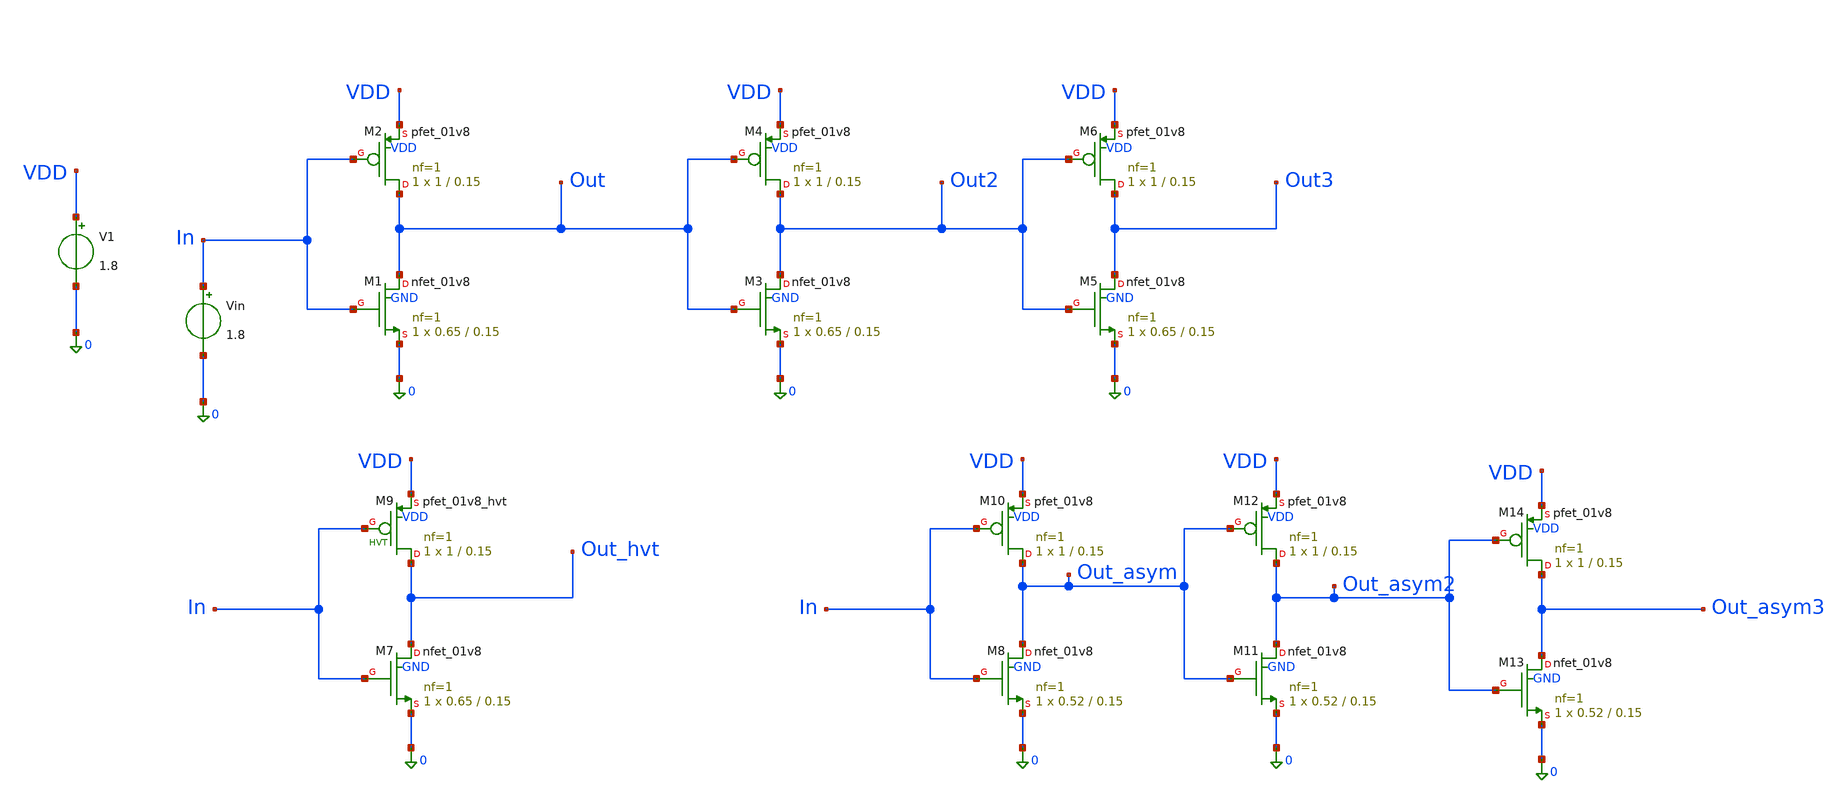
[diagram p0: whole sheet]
** sch_path: schem/inv_sizing.sch
**.subckt inv_sizing
XM1 Out In 0 GND sky130_fd_pr__nfet_01v8 L=0.15 W=0.65 nf=1 ad='int((1 + 1)/2) * 0.65 / 1 * 0.29' as='int((1 + 2)/2) * 0.65 / 1 * 0.29'
+ pd='2*int((1 + 1)/2) * (0.65 / 1 + 0.29)' ps='2*int((1 + 2)/2) * (0.65 / 1 + 0.29)' nrd='0.29 / 0.65 '
+ nrs='0.29 / 0.65 ' sa=0 sb=0 sd=0 mult=1 m=1
XM2 Out In VDD VDD sky130_fd_pr__pfet_01v8 L=0.15 W=1 nf=1 ad='int((1 + 1)/2) * 1 / 1 * 0.29' as='int((1 + 2)/2) * 1 / 1 * 0.29'
+ pd='2*int((1 + 1)/2) * (1 / 1 + 0.29)' ps='2*int((1 + 2)/2) * (1 / 1 + 0.29)' nrd='0.29 / 1 ' nrs='0.29 / 1 '
+ sa=0 sb=0 sd=0 mult=1 m=1
V1 VDD 0 1.8
Vin In 0 1.8
.save i(vin)
XM3 Out2 Out 0 GND sky130_fd_pr__nfet_01v8 L=0.15 W=0.65 nf=1 ad='int((1 + 1)/2) * 0.65 / 1 * 0.29' as='int((1 + 2)/2) * 0.65 / 1 * 0.29'
+ pd='2*int((1 + 1)/2) * (0.65 / 1 + 0.29)' ps='2*int((1 + 2)/2) * (0.65 / 1 + 0.29)' nrd='0.29 / 0.65 '
+ nrs='0.29 / 0.65 ' sa=0 sb=0 sd=0 mult=1 m=1
XM4 Out2 Out VDD VDD sky130_fd_pr__pfet_01v8 L=0.15 W=1 nf=1 ad='int((1 + 1)/2) * 1 / 1 * 0.29' as='int((1 + 2)/2) * 1 / 1 * 0.29'
+ pd='2*int((1 + 1)/2) * (1 / 1 + 0.29)' ps='2*int((1 + 2)/2) * (1 / 1 + 0.29)' nrd='0.29 / 1 ' nrs='0.29 / 1 '
+ sa=0 sb=0 sd=0 mult=1 m=1
XM5 Out3 Out2 0 GND sky130_fd_pr__nfet_01v8 L=0.15 W=0.65 nf=1 ad='int((1 + 1)/2) * 0.65 / 1 * 0.29'
+ as='int((1 + 2)/2) * 0.65 / 1 * 0.29' pd='2*int((1 + 1)/2) * (0.65 / 1 + 0.29)' ps='2*int((1 + 2)/2) * (0.65 / 1 + 0.29)'
+ nrd='0.29 / 0.65 ' nrs='0.29 / 0.65 ' sa=0 sb=0 sd=0 mult=1 m=1
XM6 Out3 Out2 VDD VDD sky130_fd_pr__pfet_01v8 L=0.15 W=1 nf=1 ad='int((1 + 1)/2) * 1 / 1 * 0.29' as='int((1 + 2)/2) * 1 / 1 * 0.29'
+ pd='2*int((1 + 1)/2) * (1 / 1 + 0.29)' ps='2*int((1 + 2)/2) * (1 / 1 + 0.29)' nrd='0.29 / 1 ' nrs='0.29 / 1 '
+ sa=0 sb=0 sd=0 mult=1 m=1
XM7 Out_hvt In 0 GND sky130_fd_pr__nfet_01v8 L=0.15 W=0.65 nf=1 ad='int((1 + 1)/2) * 0.65 / 1 * 0.29'
+ as='int((1 + 2)/2) * 0.65 / 1 * 0.29' pd='2*int((1 + 1)/2) * (0.65 / 1 + 0.29)' ps='2*int((1 + 2)/2) * (0.65 / 1 + 0.29)'
+ nrd='0.29 / 0.65 ' nrs='0.29 / 0.65 ' sa=0 sb=0 sd=0 mult=1 m=1
XM9 Out_hvt In VDD VDD sky130_fd_pr__pfet_01v8_hvt L=0.15 W=1 nf=1 ad='int((1 + 1)/2) * 1 / 1 * 0.29'
+ as='int((1 + 2)/2) * 1 / 1 * 0.29' pd='2*int((1 + 1)/2) * (1 / 1 + 0.29)' ps='2*int((1 + 2)/2) * (1 / 1 + 0.29)'
+ nrd='0.29 / 1 ' nrs='0.29 / 1 ' sa=0 sb=0 sd=0 mult=1 m=1
XM8 Out_asym In 0 GND sky130_fd_pr__nfet_01v8 L=0.15 W=0.52 nf=1 ad='int((1 + 1)/2) * 0.52 / 1 * 0.29'
+ as='int((1 + 2)/2) * 0.52 / 1 * 0.29' pd='2*int((1 + 1)/2) * (0.52 / 1 + 0.29)' ps='2*int((1 + 2)/2) * (0.52 / 1 + 0.29)'
+ nrd='0.29 / 0.52 ' nrs='0.29 / 0.52 ' sa=0 sb=0 sd=0 mult=1 m=1
XM10 Out_asym In VDD VDD sky130_fd_pr__pfet_01v8 L=0.15 W=1 nf=1 ad='int((1 + 1)/2) * 1 / 1 * 0.29' as='int((1 + 2)/2) * 1 / 1 * 0.29'
+ pd='2*int((1 + 1)/2) * (1 / 1 + 0.29)' ps='2*int((1 + 2)/2) * (1 / 1 + 0.29)' nrd='0.29 / 1 ' nrs='0.29 / 1 '
+ sa=0 sb=0 sd=0 mult=1 m=1
XM11 Out_asym2 Out_asym 0 GND sky130_fd_pr__nfet_01v8 L=0.15 W=0.52 nf=1 ad='int((1 + 1)/2) * 0.52 / 1 * 0.29'
+ as='int((1 + 2)/2) * 0.52 / 1 * 0.29' pd='2*int((1 + 1)/2) * (0.52 / 1 + 0.29)' ps='2*int((1 + 2)/2) * (0.52 / 1 + 0.29)'
+ nrd='0.29 / 0.52 ' nrs='0.29 / 0.52 ' sa=0 sb=0 sd=0 mult=1 m=1
XM12 Out_asym2 Out_asym VDD VDD sky130_fd_pr__pfet_01v8 L=0.15 W=1 nf=1 ad='int((1 + 1)/2) * 1 / 1 * 0.29'
+ as='int((1 + 2)/2) * 1 / 1 * 0.29' pd='2*int((1 + 1)/2) * (1 / 1 + 0.29)' ps='2*int((1 + 2)/2) * (1 / 1 + 0.29)'
+ nrd='0.29 / 1 ' nrs='0.29 / 1 ' sa=0 sb=0 sd=0 mult=1 m=1
XM13 Out_asym3 Out_asym2 0 GND sky130_fd_pr__nfet_01v8 L=0.15 W=0.52 nf=1 ad='int((1 + 1)/2) * 0.52 / 1 * 0.29'
+ as='int((1 + 2)/2) * 0.52 / 1 * 0.29' pd='2*int((1 + 1)/2) * (0.52 / 1 + 0.29)' ps='2*int((1 + 2)/2) * (0.52 / 1 + 0.29)'
+ nrd='0.29 / 0.52 ' nrs='0.29 / 0.52 ' sa=0 sb=0 sd=0 mult=1 m=1
XM14 Out_asym3 Out_asym2 VDD VDD sky130_fd_pr__pfet_01v8 L=0.15 W=1 nf=1 ad='int((1 + 1)/2) * 1 / 1 * 0.29'
+ as='int((1 + 2)/2) * 1 / 1 * 0.29' pd='2*int((1 + 1)/2) * (1 / 1 + 0.29)' ps='2*int((1 + 2)/2) * (1 / 1 + 0.29)'
+ nrd='0.29 / 1 ' nrs='0.29 / 1 ' sa=0 sb=0 sd=0 mult=1 m=1
**** begin user architecture code


.include inv_sizing.save
.save all
.control

dc Vin 0.0 1.8 0.01
write inv_sizing.raw

Vin in 0 ac 1.8
ac dec 200 1meg 200meg
write inv_sizing_ac.raw

.endc




.lib /home/pitchu/rtl/pdk/sky130A/libs.tech/combined/sky130.lib.spice tt


**** end user architecture code
**.ends
.end
